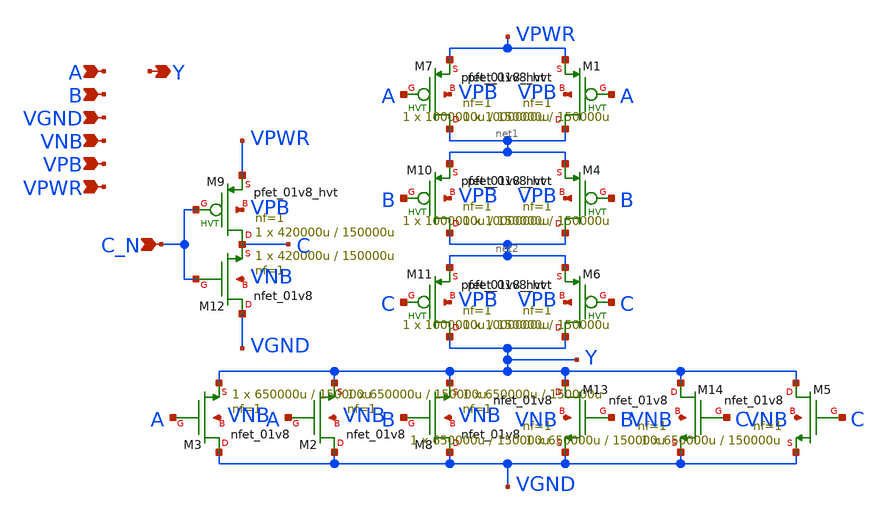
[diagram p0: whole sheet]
** sch_path: schematics/nor3b/sky130_fd_sc_hd__nor3b_2.sch
**.subckt sky130_fd_sc_hd__nor3b_2 A B C_N VGND VNB VPB VPWR Y
*.ipin A
*.ipin B
*.ipin C_N
*.ipin VGND
*.ipin VNB
*.ipin VPB
*.ipin VPWR
*.opin Y
XM1 net1 A VPWR VPB sky130_fd_pr__pfet_01v8_hvt L=150000u W=1000000u nf=1 ad='int((1 + 1)/2) * 1000000u / 1 * 0.29'
+ as='int((1 + 2)/2) * 1000000u / 1 * 0.29' pd='2*int((1 + 1)/2) * (1000000u / 1 + 0.29)' ps='2*int((1 + 2)/2) * (1000000u / 1 + 0.29)'
+ nrd='0.29 / 1000000u ' nrs='0.29 / 1000000u ' sa=0 sb=0 sd=0 mult=1 m=1
XM7 net1 A VPWR VPB sky130_fd_pr__pfet_01v8_hvt L=150000u W=1000000u nf=1 ad='int((1 + 1)/2) * 1000000u / 1 * 0.29'
+ as='int((1 + 2)/2) * 1000000u / 1 * 0.29' pd='2*int((1 + 1)/2) * (1000000u / 1 + 0.29)' ps='2*int((1 + 2)/2) * (1000000u / 1 + 0.29)'
+ nrd='0.29 / 1000000u ' nrs='0.29 / 1000000u ' sa=0 sb=0 sd=0 mult=1 m=1
XM8 VGND B Y VNB sky130_fd_pr__nfet_01v8 L=150000u W=650000u nf=1 ad='int((1 + 1)/2) * 650000u / 1 * 0.29'
+ as='int((1 + 2)/2) * 650000u / 1 * 0.29' pd='2*int((1 + 1)/2) * (650000u / 1 + 0.29)' ps='2*int((1 + 2)/2) * (650000u / 1 + 0.29)'
+ nrd='0.29 / 650000u ' nrs='0.29 / 650000u ' sa=0 sb=0 sd=0 mult=1 m=1
XM5 Y C VGND VNB sky130_fd_pr__nfet_01v8 L=150000u W=650000u nf=1 ad='int((1 + 1)/2) * 650000u / 1 * 0.29'
+ as='int((1 + 2)/2) * 650000u / 1 * 0.29' pd='2*int((1 + 1)/2) * (650000u / 1 + 0.29)' ps='2*int((1 + 2)/2) * (650000u / 1 + 0.29)'
+ nrd='0.29 / 650000u ' nrs='0.29 / 650000u ' sa=0 sb=0 sd=0 mult=1 m=1
XM4 net2 B net1 VPB sky130_fd_pr__pfet_01v8_hvt L=150000u W=1000000u nf=1 ad='int((1 + 1)/2) * 1000000u / 1 * 0.29'
+ as='int((1 + 2)/2) * 1000000u / 1 * 0.29' pd='2*int((1 + 1)/2) * (1000000u / 1 + 0.29)' ps='2*int((1 + 2)/2) * (1000000u / 1 + 0.29)'
+ nrd='0.29 / 1000000u ' nrs='0.29 / 1000000u ' sa=0 sb=0 sd=0 mult=1 m=1
XM6 Y C net2 VPB sky130_fd_pr__pfet_01v8_hvt L=150000u W=1000000u nf=1 ad='int((1 + 1)/2) * 1000000u / 1 * 0.29'
+ as='int((1 + 2)/2) * 1000000u / 1 * 0.29' pd='2*int((1 + 1)/2) * (1000000u / 1 + 0.29)' ps='2*int((1 + 2)/2) * (1000000u / 1 + 0.29)'
+ nrd='0.29 / 1000000u ' nrs='0.29 / 1000000u ' sa=0 sb=0 sd=0 mult=1 m=1
XM9 C C_N VPWR VPB sky130_fd_pr__pfet_01v8_hvt L=150000u W=420000u nf=1 ad='int((1 + 1)/2) * 420000u / 1 * 0.29'
+ as='int((1 + 2)/2) * 420000u / 1 * 0.29' pd='2*int((1 + 1)/2) * (420000u / 1 + 0.29)' ps='2*int((1 + 2)/2) * (420000u / 1 + 0.29)'
+ nrd='0.29 / 420000u ' nrs='0.29 / 420000u ' sa=0 sb=0 sd=0 mult=1 m=1
XM10 net2 B net1 VPB sky130_fd_pr__pfet_01v8_hvt L=150000u W=1000000u nf=1 ad='int((1 + 1)/2) * 1000000u / 1 * 0.29'
+ as='int((1 + 2)/2) * 1000000u / 1 * 0.29' pd='2*int((1 + 1)/2) * (1000000u / 1 + 0.29)' ps='2*int((1 + 2)/2) * (1000000u / 1 + 0.29)'
+ nrd='0.29 / 1000000u ' nrs='0.29 / 1000000u ' sa=0 sb=0 sd=0 mult=1 m=1
XM11 Y C net2 VPB sky130_fd_pr__pfet_01v8_hvt L=150000u W=1000000u nf=1 ad='int((1 + 1)/2) * 1000000u / 1 * 0.29'
+ as='int((1 + 2)/2) * 1000000u / 1 * 0.29' pd='2*int((1 + 1)/2) * (1000000u / 1 + 0.29)' ps='2*int((1 + 2)/2) * (1000000u / 1 + 0.29)'
+ nrd='0.29 / 1000000u ' nrs='0.29 / 1000000u ' sa=0 sb=0 sd=0 mult=1 m=1
XM12 VGND C_N C VNB sky130_fd_pr__nfet_01v8 L=150000u W=420000u nf=1 ad='int((1 + 1)/2) * 420000u / 1 * 0.29'
+ as='int((1 + 2)/2) * 420000u / 1 * 0.29' pd='2*int((1 + 1)/2) * (420000u / 1 + 0.29)' ps='2*int((1 + 2)/2) * (420000u / 1 + 0.29)'
+ nrd='0.29 / 420000u ' nrs='0.29 / 420000u ' sa=0 sb=0 sd=0 mult=1 m=1
XM2 VGND A Y VNB sky130_fd_pr__nfet_01v8 L=150000u W=650000u nf=1 ad='int((1 + 1)/2) * 650000u / 1 * 0.29'
+ as='int((1 + 2)/2) * 650000u / 1 * 0.29' pd='2*int((1 + 1)/2) * (650000u / 1 + 0.29)' ps='2*int((1 + 2)/2) * (650000u / 1 + 0.29)'
+ nrd='0.29 / 650000u ' nrs='0.29 / 650000u ' sa=0 sb=0 sd=0 mult=1 m=1
XM3 VGND A Y VNB sky130_fd_pr__nfet_01v8 L=150000u W=650000u nf=1 ad='int((1 + 1)/2) * 650000u / 1 * 0.29'
+ as='int((1 + 2)/2) * 650000u / 1 * 0.29' pd='2*int((1 + 1)/2) * (650000u / 1 + 0.29)' ps='2*int((1 + 2)/2) * (650000u / 1 + 0.29)'
+ nrd='0.29 / 650000u ' nrs='0.29 / 650000u ' sa=0 sb=0 sd=0 mult=1 m=1
XM13 Y B VGND VNB sky130_fd_pr__nfet_01v8 L=150000u W=650000u nf=1 ad='int((1 + 1)/2) * 650000u / 1 * 0.29'
+ as='int((1 + 2)/2) * 650000u / 1 * 0.29' pd='2*int((1 + 1)/2) * (650000u / 1 + 0.29)' ps='2*int((1 + 2)/2) * (650000u / 1 + 0.29)'
+ nrd='0.29 / 650000u ' nrs='0.29 / 650000u ' sa=0 sb=0 sd=0 mult=1 m=1
XM14 Y C VGND VNB sky130_fd_pr__nfet_01v8 L=150000u W=650000u nf=1 ad='int((1 + 1)/2) * 650000u / 1 * 0.29'
+ as='int((1 + 2)/2) * 650000u / 1 * 0.29' pd='2*int((1 + 1)/2) * (650000u / 1 + 0.29)' ps='2*int((1 + 2)/2) * (650000u / 1 + 0.29)'
+ nrd='0.29 / 650000u ' nrs='0.29 / 650000u ' sa=0 sb=0 sd=0 mult=1 m=1
**.ends
.end
